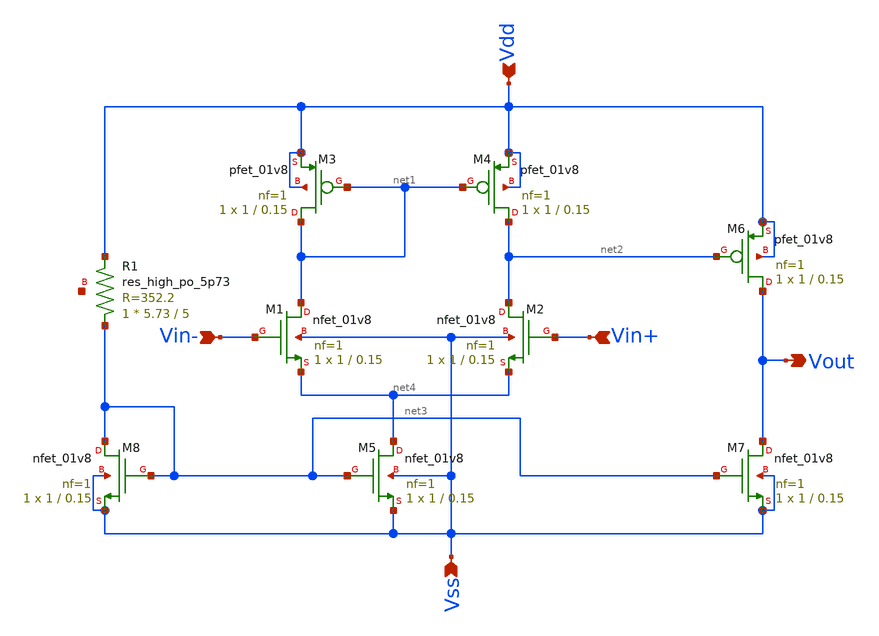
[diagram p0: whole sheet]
** sch_path: analog/schematics/bootcamp_opamp.sch
**.subckt bootcamp_opamp Vdd Vout Vin- Vin+ Vss
*.ipin Vdd
*.opin Vout
*.ipin Vin-
*.ipin Vin+
*.ipin Vss
XM1 net1 Vin- net4 Vss sky130_fd_pr__nfet_01v8 L=0.15 W=1 nf=1 ad='int((nf+1)/2) * W/nf * 0.29' as='int((nf+2)/2) * W/nf * 0.29'
+ pd='2*int((nf+1)/2) * (W/nf + 0.29)' ps='2*int((nf+2)/2) * (W/nf + 0.29)' nrd='0.29 / W' nrs='0.29 / W'
+ sa=0 sb=0 sd=0 mult=1 m=1
XM2 net2 Vin+ net4 Vss sky130_fd_pr__nfet_01v8 L=0.15 W=1 nf=1 ad='int((nf+1)/2) * W/nf * 0.29' as='int((nf+2)/2) * W/nf * 0.29'
+ pd='2*int((nf+1)/2) * (W/nf + 0.29)' ps='2*int((nf+2)/2) * (W/nf + 0.29)' nrd='0.29 / W' nrs='0.29 / W'
+ sa=0 sb=0 sd=0 mult=1 m=1
XM3 net1 net1 Vdd Vdd sky130_fd_pr__pfet_01v8 L=0.15 W=1 nf=1 ad='int((nf+1)/2) * W/nf * 0.29' as='int((nf+2)/2) * W/nf * 0.29'
+ pd='2*int((nf+1)/2) * (W/nf + 0.29)' ps='2*int((nf+2)/2) * (W/nf + 0.29)' nrd='0.29 / W' nrs='0.29 / W'
+ sa=0 sb=0 sd=0 mult=1 m=1
XM4 net2 net1 Vdd Vdd sky130_fd_pr__pfet_01v8 L=0.15 W=1 nf=1 ad='int((nf+1)/2) * W/nf * 0.29' as='int((nf+2)/2) * W/nf * 0.29'
+ pd='2*int((nf+1)/2) * (W/nf + 0.29)' ps='2*int((nf+2)/2) * (W/nf + 0.29)' nrd='0.29 / W' nrs='0.29 / W'
+ sa=0 sb=0 sd=0 mult=1 m=1
XM5 net4 net3 Vss Vss sky130_fd_pr__nfet_01v8 L=0.15 W=1 nf=1 ad='int((nf+1)/2) * W/nf * 0.29' as='int((nf+2)/2) * W/nf * 0.29'
+ pd='2*int((nf+1)/2) * (W/nf + 0.29)' ps='2*int((nf+2)/2) * (W/nf + 0.29)' nrd='0.29 / W' nrs='0.29 / W'
+ sa=0 sb=0 sd=0 mult=1 m=1
XM6 Vout net2 Vdd Vdd sky130_fd_pr__pfet_01v8 L=0.15 W=1 nf=1 ad='int((nf+1)/2) * W/nf * 0.29' as='int((nf+2)/2) * W/nf * 0.29'
+ pd='2*int((nf+1)/2) * (W/nf + 0.29)' ps='2*int((nf+2)/2) * (W/nf + 0.29)' nrd='0.29 / W' nrs='0.29 / W'
+ sa=0 sb=0 sd=0 mult=1 m=1
XM7 Vout net3 Vss Vss sky130_fd_pr__nfet_01v8 L=0.15 W=1 nf=1 ad='int((nf+1)/2) * W/nf * 0.29' as='int((nf+2)/2) * W/nf * 0.29'
+ pd='2*int((nf+1)/2) * (W/nf + 0.29)' ps='2*int((nf+2)/2) * (W/nf + 0.29)' nrd='0.29 / W' nrs='0.29 / W'
+ sa=0 sb=0 sd=0 mult=1 m=1
XM8 net3 net3 Vss Vss sky130_fd_pr__nfet_01v8 L=0.15 W=1 nf=1 ad='int((nf+1)/2) * W/nf * 0.29' as='int((nf+2)/2) * W/nf * 0.29'
+ pd='2*int((nf+1)/2) * (W/nf + 0.29)' ps='2*int((nf+2)/2) * (W/nf + 0.29)' nrd='0.29 / W' nrs='0.29 / W'
+ sa=0 sb=0 sd=0 mult=1 m=1
XR1 net3 Vdd net5 sky130_fd_pr__res_high_po_5p73 L=5 mult=1 m=1
**.ends
.end
